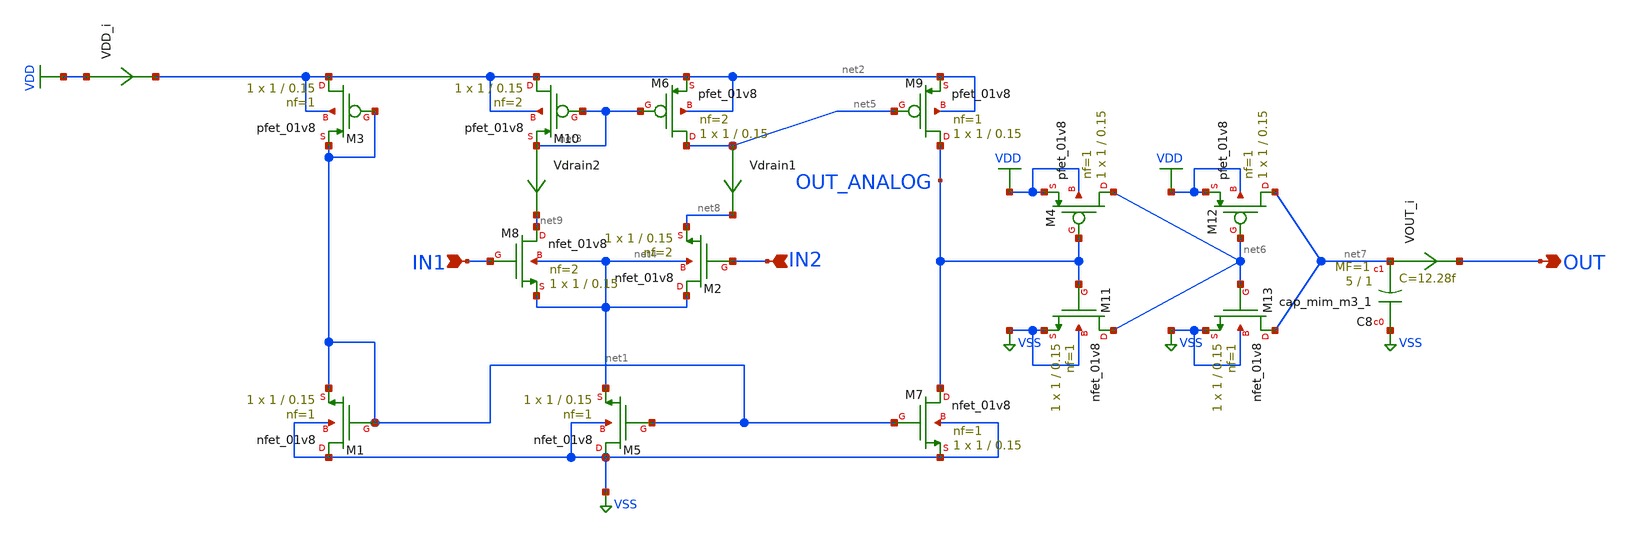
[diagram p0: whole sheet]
** sch_path: 1bit_adc/comparator_for_layout.sch
**.subckt comparator_for_layout IN1 IN2 OUT
*.ipin IN1
*.ipin IN2
*.opin OUT
XM9 OUT_ANALOG net5 net2 net2 sky130_fd_pr__pfet_01v8 L=0.15 W=1 nf=1 ad='int((nf+1)/2) * W/nf * 0.29'
+ as='int((nf+2)/2) * W/nf * 0.29' pd='2*int((nf+1)/2) * (W/nf + 0.29)' ps='2*int((nf+2)/2) * (W/nf + 0.29)'
+ nrd='0.29 / W' nrs='0.29 / W' sa=0 sb=0 sd=0 mult=1 m=1
XM6 net5 net3 net2 net2 sky130_fd_pr__pfet_01v8 L=0.15 W=1 nf=2 ad='int((nf+1)/2) * W/nf * 0.29' as='int((nf+2)/2) * W/nf * 0.29'
+ pd='2*int((nf+1)/2) * (W/nf + 0.29)' ps='2*int((nf+2)/2) * (W/nf + 0.29)' nrd='0.29 / W' nrs='0.29 / W'
+ sa=0 sb=0 sd=0 mult=1 m=1
XM10 net2 net3 net3 net2 sky130_fd_pr__pfet_01v8 L=0.15 W=1 nf=2 ad='int((nf+1)/2) * W/nf * 0.29' as='int((nf+2)/2) * W/nf * 0.29'
+ pd='2*int((nf+1)/2) * (W/nf + 0.29)' ps='2*int((nf+2)/2) * (W/nf + 0.29)' nrd='0.29 / W' nrs='0.29 / W'
+ sa=0 sb=0 sd=0 mult=1 m=1
XM3 net2 net1 net1 net2 sky130_fd_pr__pfet_01v8 L=0.15 W=1 nf=1 ad='int((nf+1)/2) * W/nf * 0.29' as='int((nf+2)/2) * W/nf * 0.29'
+ pd='2*int((nf+1)/2) * (W/nf + 0.29)' ps='2*int((nf+2)/2) * (W/nf + 0.29)' nrd='0.29 / W' nrs='0.29 / W'
+ sa=0 sb=0 sd=0 mult=1 m=1
XM4 net6 OUT_ANALOG VDD VDD sky130_fd_pr__pfet_01v8 L=0.15 W=1 nf=1 ad='int((nf+1)/2) * W/nf * 0.29'
+ as='int((nf+2)/2) * W/nf * 0.29' pd='2*int((nf+1)/2) * (W/nf + 0.29)' ps='2*int((nf+2)/2) * (W/nf + 0.29)'
+ nrd='0.29 / W' nrs='0.29 / W' sa=0 sb=0 sd=0 mult=1 m=1
XM12 net7 net6 VDD VDD sky130_fd_pr__pfet_01v8 L=0.15 W=1 nf=1 ad='int((nf+1)/2) * W/nf * 0.29' as='int((nf+2)/2) * W/nf * 0.29'
+ pd='2*int((nf+1)/2) * (W/nf + 0.29)' ps='2*int((nf+2)/2) * (W/nf + 0.29)' nrd='0.29 / W' nrs='0.29 / W'
+ sa=0 sb=0 sd=0 mult=1 m=1
Vdrain1 net5 net8 0
.save i(vdrain1)
Vdrain2 net3 net9 0
.save i(vdrain2)
VDD_i VDD net2 0
.save i(vdd_i)
VOUT_i net7 OUT 0
.save i(vout_i)
XM2 net4 IN2 net8 net4 sky130_fd_pr__nfet_01v8 L=0.15 W=1 nf=2 ad='int((nf+1)/2) * W/nf * 0.29' as='int((nf+2)/2) * W/nf * 0.29'
+ pd='2*int((nf+1)/2) * (W/nf + 0.29)' ps='2*int((nf+2)/2) * (W/nf + 0.29)' nrd='0.29 / W' nrs='0.29 / W'
+ sa=0 sb=0 sd=0 mult=1 m=1
XM1 VSS net1 net1 VSS sky130_fd_pr__nfet_01v8 L=0.15 W=1 nf=1 ad='int((nf+1)/2) * W/nf * 0.29' as='int((nf+2)/2) * W/nf * 0.29'
+ pd='2*int((nf+1)/2) * (W/nf + 0.29)' ps='2*int((nf+2)/2) * (W/nf + 0.29)' nrd='0.29 / W' nrs='0.29 / W'
+ sa=0 sb=0 sd=0 mult=1 m=1
XM5 VSS net1 net4 VSS sky130_fd_pr__nfet_01v8 L=0.15 W=1 nf=1 ad='int((nf+1)/2) * W/nf * 0.29' as='int((nf+2)/2) * W/nf * 0.29'
+ pd='2*int((nf+1)/2) * (W/nf + 0.29)' ps='2*int((nf+2)/2) * (W/nf + 0.29)' nrd='0.29 / W' nrs='0.29 / W'
+ sa=0 sb=0 sd=0 mult=1 m=1
XM7 OUT_ANALOG net1 VSS VSS sky130_fd_pr__nfet_01v8 L=0.15 W=1 nf=1 ad='int((nf+1)/2) * W/nf * 0.29'
+ as='int((nf+2)/2) * W/nf * 0.29' pd='2*int((nf+1)/2) * (W/nf + 0.29)' ps='2*int((nf+2)/2) * (W/nf + 0.29)'
+ nrd='0.29 / W' nrs='0.29 / W' sa=0 sb=0 sd=0 mult=1 m=1
XM8 net9 IN1 net4 net4 sky130_fd_pr__nfet_01v8 L=0.15 W=1 nf=2 ad='int((nf+1)/2) * W/nf * 0.29' as='int((nf+2)/2) * W/nf * 0.29'
+ pd='2*int((nf+1)/2) * (W/nf + 0.29)' ps='2*int((nf+2)/2) * (W/nf + 0.29)' nrd='0.29 / W' nrs='0.29 / W'
+ sa=0 sb=0 sd=0 mult=1 m=1
XM11 net6 OUT_ANALOG VSS VSS sky130_fd_pr__nfet_01v8 L=0.15 W=1 nf=1 ad='int((nf+1)/2) * W/nf * 0.29'
+ as='int((nf+2)/2) * W/nf * 0.29' pd='2*int((nf+1)/2) * (W/nf + 0.29)' ps='2*int((nf+2)/2) * (W/nf + 0.29)'
+ nrd='0.29 / W' nrs='0.29 / W' sa=0 sb=0 sd=0 mult=1 m=1
XM13 net7 net6 VSS VSS sky130_fd_pr__nfet_01v8 L=0.15 W=1 nf=1 ad='int((nf+1)/2) * W/nf * 0.29' as='int((nf+2)/2) * W/nf * 0.29'
+ pd='2*int((nf+1)/2) * (W/nf + 0.29)' ps='2*int((nf+2)/2) * (W/nf + 0.29)' nrd='0.29 / W' nrs='0.29 / W'
+ sa=0 sb=0 sd=0 mult=1 m=1
XC8 VSS net7 sky130_fd_pr__cap_mim_m3_1 W=5 L=1 MF=1 m=1
**** begin user architecture code

** opencircuitdesign pdks install
.lib $::SKYWATER_MODELS/sky130.lib.spice tt
.include $::SKYWATER_STDCELLS/sky130_fd_sc_hd.spice
.include /foss/pdks/sky130A/libs.tech/xschem/sky130_stdcells/
.include /foss/pdks/sky130A/libs.tech/xschem/sky130_fd_pr/



.options gmin=1e-12
.param vdd=1.8
.param clk=500n
VVDD VDD 0 DC vdd
VIN1 IN1 0 SIN(1 0.5 450k 5n)
VIN2 IN2 0 SIN(1 0.5 200k 5n)
VGND VSS 0 DC 0
.tran {clk/4} {clk*100}
.control
save all

run
tran {clk/10} {clk*10}

remzerovec
write comparator_for_layout.raw all
*set appendwrite

*echo AC
*reset
*save all
*ac dec 50 5k 100k

*display
*write 1bit_adc.raw all



echo AMONG US
shell pwd

.endc
.end


**** end user architecture code
**.ends
.GLOBAL VSS
.GLOBAL VDD
.end
